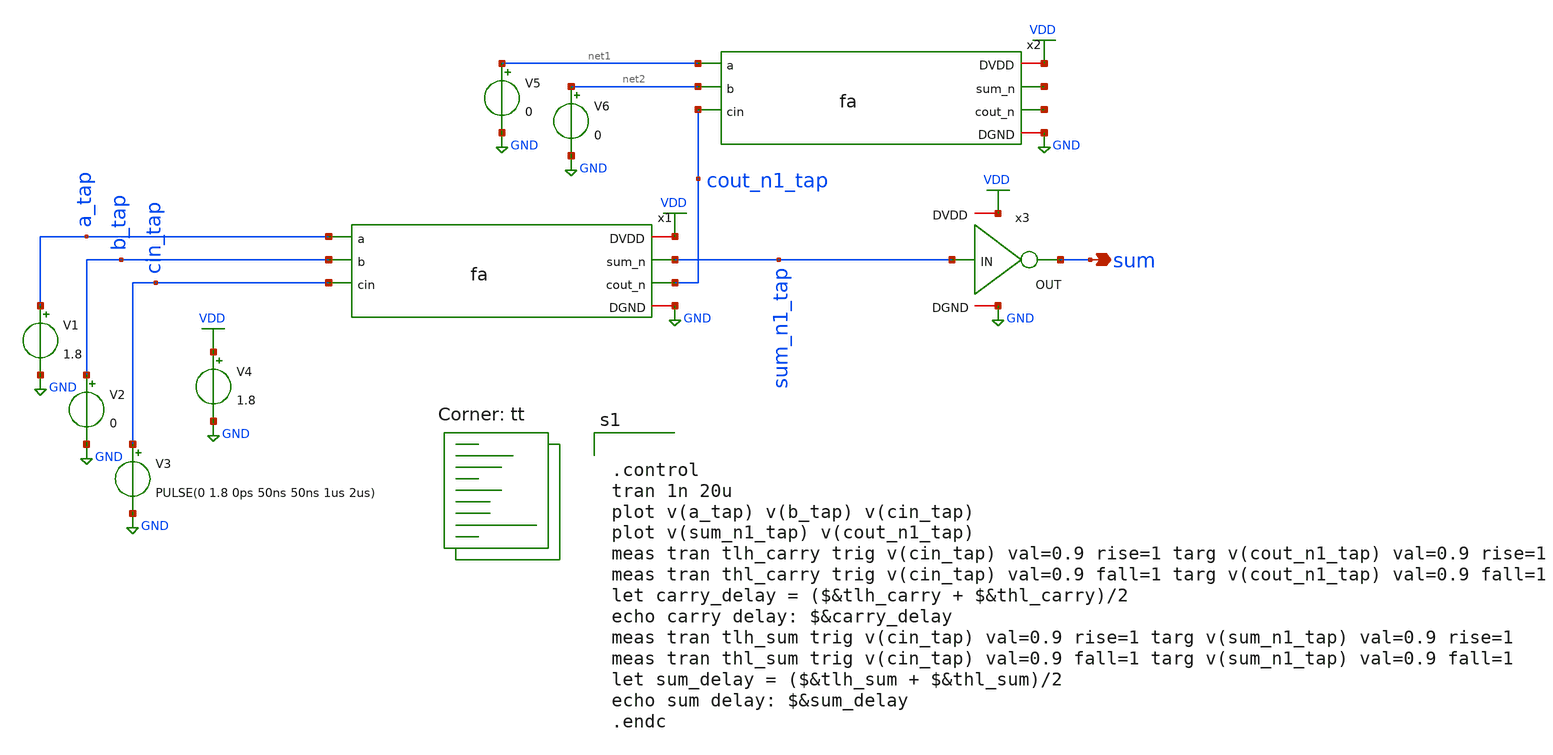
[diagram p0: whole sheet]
** sch_path: tut6/sim/pre_layout/fa_tb.sch
**.subckt fa_tb sum
*.opin sum
x1 VDD a_tap b_tap cin_tap sum_n1_tap cout_n1_tap GND fa
x2 VDD net1 net2 cout_n1_tap net3 net4 GND fa
x3 VDD sum sum_n1_tap GND inv
V1 a_tap GND 1.8
V2 b_tap GND 0
V3 cin_tap GND PULSE(0 1.8 0ps 50ns 50ns 1us 2us)
V4 VDD GND 1.8
V5 net1 GND 0
V6 net2 GND 0
**** begin user architecture code


.control
tran 1n 20u
plot v(a_tap) v(b_tap) v(cin_tap)
plot v(sum_n1_tap) v(cout_n1_tap)
meas tran tlh_carry trig v(cin_tap) val=0.9 rise=1 targ v(cout_n1_tap) val=0.9 rise=1
meas tran thl_carry trig v(cin_tap) val=0.9 fall=1 targ v(cout_n1_tap) val=0.9 fall=1
let carry_delay = ($&tlh_carry + $&thl_carry)/2
echo carry delay: $&carry_delay
meas tran tlh_sum trig v(cin_tap) val=0.9 rise=1 targ v(sum_n1_tap) val=0.9 rise=1
meas tran thl_sum trig v(cin_tap) val=0.9 fall=1 targ v(sum_n1_tap) val=0.9 fall=1
let sum_delay = ($&tlh_sum + $&thl_sum)/2
echo sum delay: $&sum_delay
.endc


.lib $::SKYWATER_MODELS/sky130.lib.spice tt
**** end user architecture code
**.ends

* expanding   symbol:  fa.sym # of pins=7
** sym_path: tut6/sim/pre_layout/fa.sym
** sch_path: tut6/sim/pre_layout/fa.sch
.subckt fa DVDD a b cin sum_n cout_n DGND
*.iopin DVDD
*.iopin DGND
*.opin sum_n
*.opin cout_n
*.ipin a
*.ipin b
*.ipin cin
XM3 net5 a DGND DGND sky130_fd_pr__nfet_01v8 L=0.15 W=1.68 nf=1 ad='int((nf+1)/2) * W/nf * 0.29' as='int((nf+2)/2) * W/nf * 0.29'
+ pd='2*int((nf+1)/2) * (W/nf + 0.29)' ps='2*int((nf+2)/2) * (W/nf + 0.29)' nrd='0.29 / W' nrs='0.29 / W'
+ sa=0 sb=0 sd=0 mult=1 m=1
XM7 cout_n cin net5 DGND sky130_fd_pr__nfet_01v8 L=0.15 W=0.84 nf=1 ad='int((nf+1)/2) * W/nf * 0.29'
+ as='int((nf+2)/2) * W/nf * 0.29' pd='2*int((nf+1)/2) * (W/nf + 0.29)' ps='2*int((nf+2)/2) * (W/nf + 0.29)'
+ nrd='0.29 / W' nrs='0.29 / W' sa=0 sb=0 sd=0 mult=1 m=1
XM8 net5 b DGND DGND sky130_fd_pr__nfet_01v8 L=0.15 W=1.68 nf=1 ad='int((nf+1)/2) * W/nf * 0.29' as='int((nf+2)/2) * W/nf * 0.29'
+ pd='2*int((nf+1)/2) * (W/nf + 0.29)' ps='2*int((nf+2)/2) * (W/nf + 0.29)' nrd='0.29 / W' nrs='0.29 / W'
+ sa=0 sb=0 sd=0 mult=1 m=1
XM9 net2 a DGND DGND sky130_fd_pr__nfet_01v8 L=0.15 W=0.42 nf=1 ad='int((nf+1)/2) * W/nf * 0.29' as='int((nf+2)/2) * W/nf * 0.29'
+ pd='2*int((nf+1)/2) * (W/nf + 0.29)' ps='2*int((nf+2)/2) * (W/nf + 0.29)' nrd='0.29 / W' nrs='0.29 / W'
+ sa=0 sb=0 sd=0 mult=1 m=1
XM10 net2 b DGND DGND sky130_fd_pr__nfet_01v8 L=0.15 W=0.42 nf=1 ad='int((nf+1)/2) * W/nf * 0.29' as='int((nf+2)/2) * W/nf * 0.29'
+ pd='2*int((nf+1)/2) * (W/nf + 0.29)' ps='2*int((nf+2)/2) * (W/nf + 0.29)' nrd='0.29 / W' nrs='0.29 / W'
+ sa=0 sb=0 sd=0 mult=1 m=1
XM11 net2 cin DGND DGND sky130_fd_pr__nfet_01v8 L=0.15 W=0.42 nf=1 ad='int((nf+1)/2) * W/nf * 0.29' as='int((nf+2)/2) * W/nf * 0.29'
+ pd='2*int((nf+1)/2) * (W/nf + 0.29)' ps='2*int((nf+2)/2) * (W/nf + 0.29)' nrd='0.29 / W' nrs='0.29 / W'
+ sa=0 sb=0 sd=0 mult=1 m=1
XM12 sum_n cout_n net2 DGND sky130_fd_pr__nfet_01v8 L=0.15 W=0.42 nf=1 ad='int((nf+1)/2) * W/nf * 0.29'
+ as='int((nf+2)/2) * W/nf * 0.29' pd='2*int((nf+1)/2) * (W/nf + 0.29)' ps='2*int((nf+2)/2) * (W/nf + 0.29)'
+ nrd='0.29 / W' nrs='0.29 / W' sa=0 sb=0 sd=0 mult=1 m=1
XM13 sum_n cin net7 DGND sky130_fd_pr__nfet_01v8 L=0.15 W=0.42 nf=1 ad='int((nf+1)/2) * W/nf * 0.29'
+ as='int((nf+2)/2) * W/nf * 0.29' pd='2*int((nf+1)/2) * (W/nf + 0.29)' ps='2*int((nf+2)/2) * (W/nf + 0.29)'
+ nrd='0.29 / W' nrs='0.29 / W' sa=0 sb=0 sd=0 mult=1 m=1
XM14 net7 b net8 DGND sky130_fd_pr__nfet_01v8 L=0.15 W=0.42 nf=1 ad='int((nf+1)/2) * W/nf * 0.29' as='int((nf+2)/2) * W/nf * 0.29'
+ pd='2*int((nf+1)/2) * (W/nf + 0.29)' ps='2*int((nf+2)/2) * (W/nf + 0.29)' nrd='0.29 / W' nrs='0.29 / W'
+ sa=0 sb=0 sd=0 mult=1 m=1
XM15 net8 a DGND DGND sky130_fd_pr__nfet_01v8 L=0.15 W=0.42 nf=1 ad='int((nf+1)/2) * W/nf * 0.29' as='int((nf+2)/2) * W/nf * 0.29'
+ pd='2*int((nf+1)/2) * (W/nf + 0.29)' ps='2*int((nf+2)/2) * (W/nf + 0.29)' nrd='0.29 / W' nrs='0.29 / W'
+ sa=0 sb=0 sd=0 mult=1 m=1
XM16 net3 a DVDD DVDD sky130_fd_pr__pfet_01v8 L=0.15 W=1.68 nf=1 ad='int((nf+1)/2) * W/nf * 0.29' as='int((nf+2)/2) * W/nf * 0.29'
+ pd='2*int((nf+1)/2) * (W/nf + 0.29)' ps='2*int((nf+2)/2) * (W/nf + 0.29)' nrd='0.29 / W' nrs='0.29 / W'
+ sa=0 sb=0 sd=0 mult=1 m=1
XM18 net4 a DVDD DVDD sky130_fd_pr__pfet_01v8 L=0.15 W=3.36 nf=1 ad='int((nf+1)/2) * W/nf * 0.29' as='int((nf+2)/2) * W/nf * 0.29'
+ pd='2*int((nf+1)/2) * (W/nf + 0.29)' ps='2*int((nf+2)/2) * (W/nf + 0.29)' nrd='0.29 / W' nrs='0.29 / W'
+ sa=0 sb=0 sd=0 mult=1 m=1
XM22 cout_n cin net4 DVDD sky130_fd_pr__pfet_01v8 L=0.15 W=1.68 nf=1 ad='int((nf+1)/2) * W/nf * 0.29'
+ as='int((nf+2)/2) * W/nf * 0.29' pd='2*int((nf+1)/2) * (W/nf + 0.29)' ps='2*int((nf+2)/2) * (W/nf + 0.29)'
+ nrd='0.29 / W' nrs='0.29 / W' sa=0 sb=0 sd=0 mult=1 m=1
XM23 net4 b DVDD DVDD sky130_fd_pr__pfet_01v8 L=0.15 W=3.36 nf=1 ad='int((nf+1)/2) * W/nf * 0.29' as='int((nf+2)/2) * W/nf * 0.29'
+ pd='2*int((nf+1)/2) * (W/nf + 0.29)' ps='2*int((nf+2)/2) * (W/nf + 0.29)' nrd='0.29 / W' nrs='0.29 / W'
+ sa=0 sb=0 sd=0 mult=1 m=1
XM25 sum_n cin net9 DVDD sky130_fd_pr__pfet_01v8 L=0.15 W=0.42 nf=1 ad='int((nf+1)/2) * W/nf * 0.29'
+ as='int((nf+2)/2) * W/nf * 0.29' pd='2*int((nf+1)/2) * (W/nf + 0.29)' ps='2*int((nf+2)/2) * (W/nf + 0.29)'
+ nrd='0.29 / W' nrs='0.29 / W' sa=0 sb=0 sd=0 mult=1 m=1
XM26 net9 b net10 DVDD sky130_fd_pr__pfet_01v8 L=0.15 W=0.42 nf=1 ad='int((nf+1)/2) * W/nf * 0.29' as='int((nf+2)/2) * W/nf * 0.29'
+ pd='2*int((nf+1)/2) * (W/nf + 0.29)' ps='2*int((nf+2)/2) * (W/nf + 0.29)' nrd='0.29 / W' nrs='0.29 / W'
+ sa=0 sb=0 sd=0 mult=1 m=1
XM27 net10 a DVDD DVDD sky130_fd_pr__pfet_01v8 L=0.15 W=0.42 nf=1 ad='int((nf+1)/2) * W/nf * 0.29' as='int((nf+2)/2) * W/nf * 0.29'
+ pd='2*int((nf+1)/2) * (W/nf + 0.29)' ps='2*int((nf+2)/2) * (W/nf + 0.29)' nrd='0.29 / W' nrs='0.29 / W'
+ sa=0 sb=0 sd=0 mult=1 m=1
XM1 net6 a DGND DGND sky130_fd_pr__nfet_01v8 L=0.15 W=0.84 nf=1 ad='int((nf+1)/2) * W/nf * 0.29' as='int((nf+2)/2) * W/nf * 0.29'
+ pd='2*int((nf+1)/2) * (W/nf + 0.29)' ps='2*int((nf+2)/2) * (W/nf + 0.29)' nrd='0.29 / W' nrs='0.29 / W'
+ sa=0 sb=0 sd=0 mult=1 m=1
XM2 cout_n b net3 DVDD sky130_fd_pr__pfet_01v8 L=0.15 W=1.68 nf=1 ad='int((nf+1)/2) * W/nf * 0.29' as='int((nf+2)/2) * W/nf * 0.29'
+ pd='2*int((nf+1)/2) * (W/nf + 0.29)' ps='2*int((nf+2)/2) * (W/nf + 0.29)' nrd='0.29 / W' nrs='0.29 / W'
+ sa=0 sb=0 sd=0 mult=1 m=1
XM4 cout_n b net6 DGND sky130_fd_pr__nfet_01v8 L=0.15 W=0.84 nf=1 ad='int((nf+1)/2) * W/nf * 0.29' as='int((nf+2)/2) * W/nf * 0.29'
+ pd='2*int((nf+1)/2) * (W/nf + 0.29)' ps='2*int((nf+2)/2) * (W/nf + 0.29)' nrd='0.29 / W' nrs='0.29 / W'
+ sa=0 sb=0 sd=0 mult=1 m=1
XM5 net1 a DVDD DVDD sky130_fd_pr__pfet_01v8 L=0.15 W=0.42 nf=1 ad='int((nf+1)/2) * W/nf * 0.29' as='int((nf+2)/2) * W/nf * 0.29'
+ pd='2*int((nf+1)/2) * (W/nf + 0.29)' ps='2*int((nf+2)/2) * (W/nf + 0.29)' nrd='0.29 / W' nrs='0.29 / W'
+ sa=0 sb=0 sd=0 mult=1 m=1
XM6 net1 b DVDD DVDD sky130_fd_pr__pfet_01v8 L=0.15 W=0.42 nf=1 ad='int((nf+1)/2) * W/nf * 0.29' as='int((nf+2)/2) * W/nf * 0.29'
+ pd='2*int((nf+1)/2) * (W/nf + 0.29)' ps='2*int((nf+2)/2) * (W/nf + 0.29)' nrd='0.29 / W' nrs='0.29 / W'
+ sa=0 sb=0 sd=0 mult=1 m=1
XM17 net1 cin DVDD DVDD sky130_fd_pr__pfet_01v8 L=0.15 W=0.42 nf=1 ad='int((nf+1)/2) * W/nf * 0.29' as='int((nf+2)/2) * W/nf * 0.29'
+ pd='2*int((nf+1)/2) * (W/nf + 0.29)' ps='2*int((nf+2)/2) * (W/nf + 0.29)' nrd='0.29 / W' nrs='0.29 / W'
+ sa=0 sb=0 sd=0 mult=1 m=1
XM19 sum_n cout_n net1 DVDD sky130_fd_pr__pfet_01v8 L=0.15 W=0.42 nf=1 ad='int((nf+1)/2) * W/nf * 0.29'
+ as='int((nf+2)/2) * W/nf * 0.29' pd='2*int((nf+1)/2) * (W/nf + 0.29)' ps='2*int((nf+2)/2) * (W/nf + 0.29)'
+ nrd='0.29 / W' nrs='0.29 / W' sa=0 sb=0 sd=0 mult=1 m=1
.ends


* expanding   symbol:  /home/ee24s053/ee5311-2025/tut5/inv/cell/subcircuit/inv.sym # of pins=4
** sym_path: tut5/inv/prim/inv.sym
** sch_path: tut5/inv/prim/inv.sch
.subckt inv DVDD OUT IN DGND
*.iopin DVDD
*.iopin DGND
*.opin OUT
*.ipin IN
XM1 OUT IN DVDD DVDD sky130_fd_pr__pfet_01v8 L=0.15 W=0.84 nf=1 ad='int((nf+1)/2) * W/nf * 0.29' as='int((nf+2)/2) * W/nf * 0.29'
+ pd='2*int((nf+1)/2) * (W/nf + 0.29)' ps='2*int((nf+2)/2) * (W/nf + 0.29)' nrd='0.29 / W' nrs='0.29 / W'
+ sa=0 sb=0 sd=0 mult=1 m=1
XM2 OUT IN DGND DGND sky130_fd_pr__nfet_01v8 L=0.15 W=0.42 nf=1 ad='int((nf+1)/2) * W/nf * 0.29' as='int((nf+2)/2) * W/nf * 0.29'
+ pd='2*int((nf+1)/2) * (W/nf + 0.29)' ps='2*int((nf+2)/2) * (W/nf + 0.29)' nrd='0.29 / W' nrs='0.29 / W'
+ sa=0 sb=0 sd=0 mult=1 m=1
.ends

.GLOBAL GND
.GLOBAL VDD
.end
